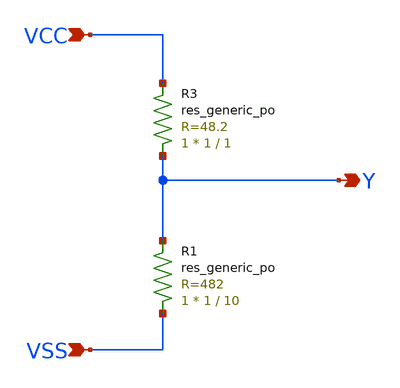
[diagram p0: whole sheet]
** sch_path: xschem/vDivider_3.sch
**.subckt vDivider_3 VCC VSS Y
*.ipin VCC
*.ipin VSS
*.opin Y
XR3 Y VCC sky130_fd_pr__res_generic_po W=1 L=1 m=1
XR1 VSS Y sky130_fd_pr__res_generic_po W=1 L=10 m=1
**.ends
.end
